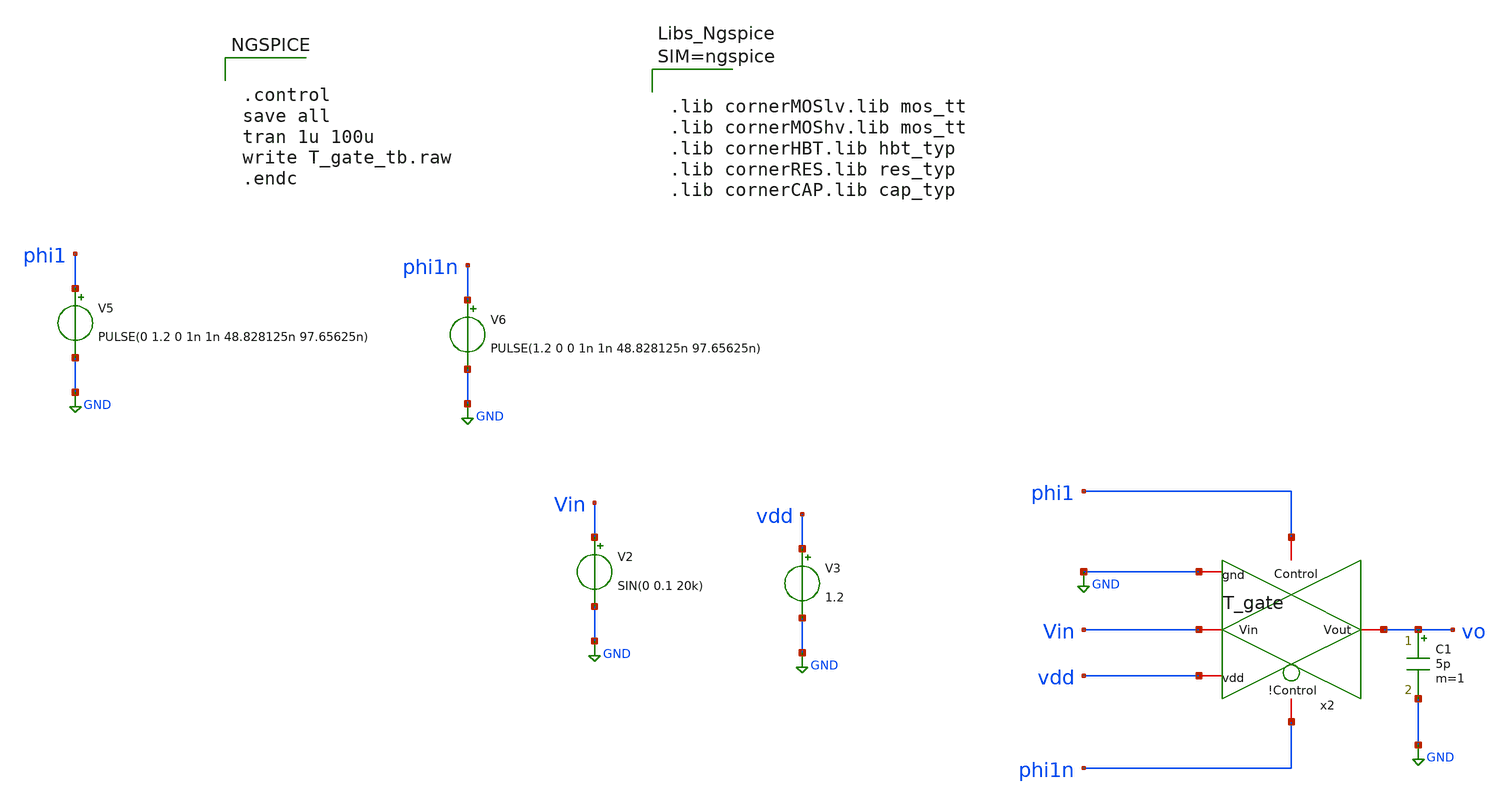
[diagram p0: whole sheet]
** sch_path: xschem/T_gate_tb.sch
**.subckt T_gate_tb
x2 phi1n Vin vo GND phi1 vdd T_gate
V3 vdd GND 1.2
V5 phi1 GND PULSE(0 1.2 0 1n 1n 48.828125n 97.65625n)
V6 phi1n GND PULSE(1.2 0 0 1n 1n 48.828125n 97.65625n)
V2 Vin GND SIN(0 0.1 20k)
C1 vo GND 5p m=1
**** begin user architecture code



.lib cornerMOSlv.lib mos_tt
.lib cornerMOShv.lib mos_tt
.lib cornerHBT.lib hbt_typ
.lib cornerRES.lib res_typ
.lib cornerCAP.lib cap_typ





.control
save all
tran 1u 100u
write T_gate_tb.raw
.endc


**** end user architecture code
**.ends

* expanding   symbol:
*+  /home/designer/shared/IHP-AnalogAcademy/modules/module_3_8_bit_SAR_ADC/part_2_digital_comps/T_gate/schematic/T_gate.sym # of pins=6
** sym_path: /home/designer/shared/IHP-AnalogAcademy/modules/module_3_8_bit_SAR_ADC/part_2_digital_comps/T_gate/schematic/T_gate.sym
** sch_path: /home/designer/shared/IHP-AnalogAcademy/modules/module_3_8_bit_SAR_ADC/part_2_digital_comps/T_gate/schematic/T_gate.sch
.subckt T_gate !Control Vin Vout gnd Control vdd
*.iopin Vout
*.iopin Vin
*.iopin !Control
*.iopin Control
*.iopin gnd
*.iopin vdd
XM1 Vin Control Vout gnd sg13_lv_nmos w=1u l=0.13u ng=1 m=1 mm_ok=1
XM2 Vout !Control Vin vdd sg13_lv_pmos w=3u l=0.13u ng=1 m=1 mm_ok=1
.ends

.GLOBAL GND
.end
